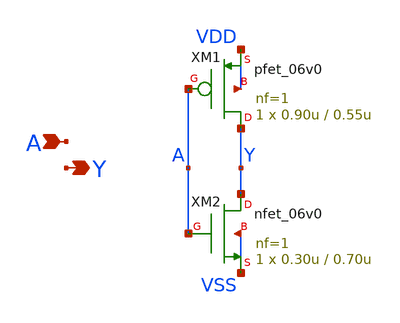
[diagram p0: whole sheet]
** sch_path: designs/libs/core_analog/digital/digital_inv_1.sch
**.subckt digital_inv_1 A Y
*.ipin A
*.opin Y
XM1 Y A VDD VDD pfet_06v0 L=0.55u W=0.90u nf=1 ad='int((nf+1)/2) * W/nf * 0.18u' as='int((nf+2)/2) * W/nf * 0.18u'
+ pd='2*int((nf+1)/2) * (W/nf + 0.18u)' ps='2*int((nf+2)/2) * (W/nf + 0.18u)' nrd='0.18u / W' nrs='0.18u / W'
+ sa=0 sb=0 sd=0 m=1
XM2 Y A VSS VSS nfet_06v0 L=0.70u W=0.30u nf=1 ad='int((nf+1)/2) * W/nf * 0.18u' as='int((nf+2)/2) * W/nf * 0.18u'
+ pd='2*int((nf+1)/2) * (W/nf + 0.18u)' ps='2*int((nf+2)/2) * (W/nf + 0.18u)' nrd='0.18u / W' nrs='0.18u / W'
+ sa=0 sb=0 sd=0 m=1
**.ends
.end
